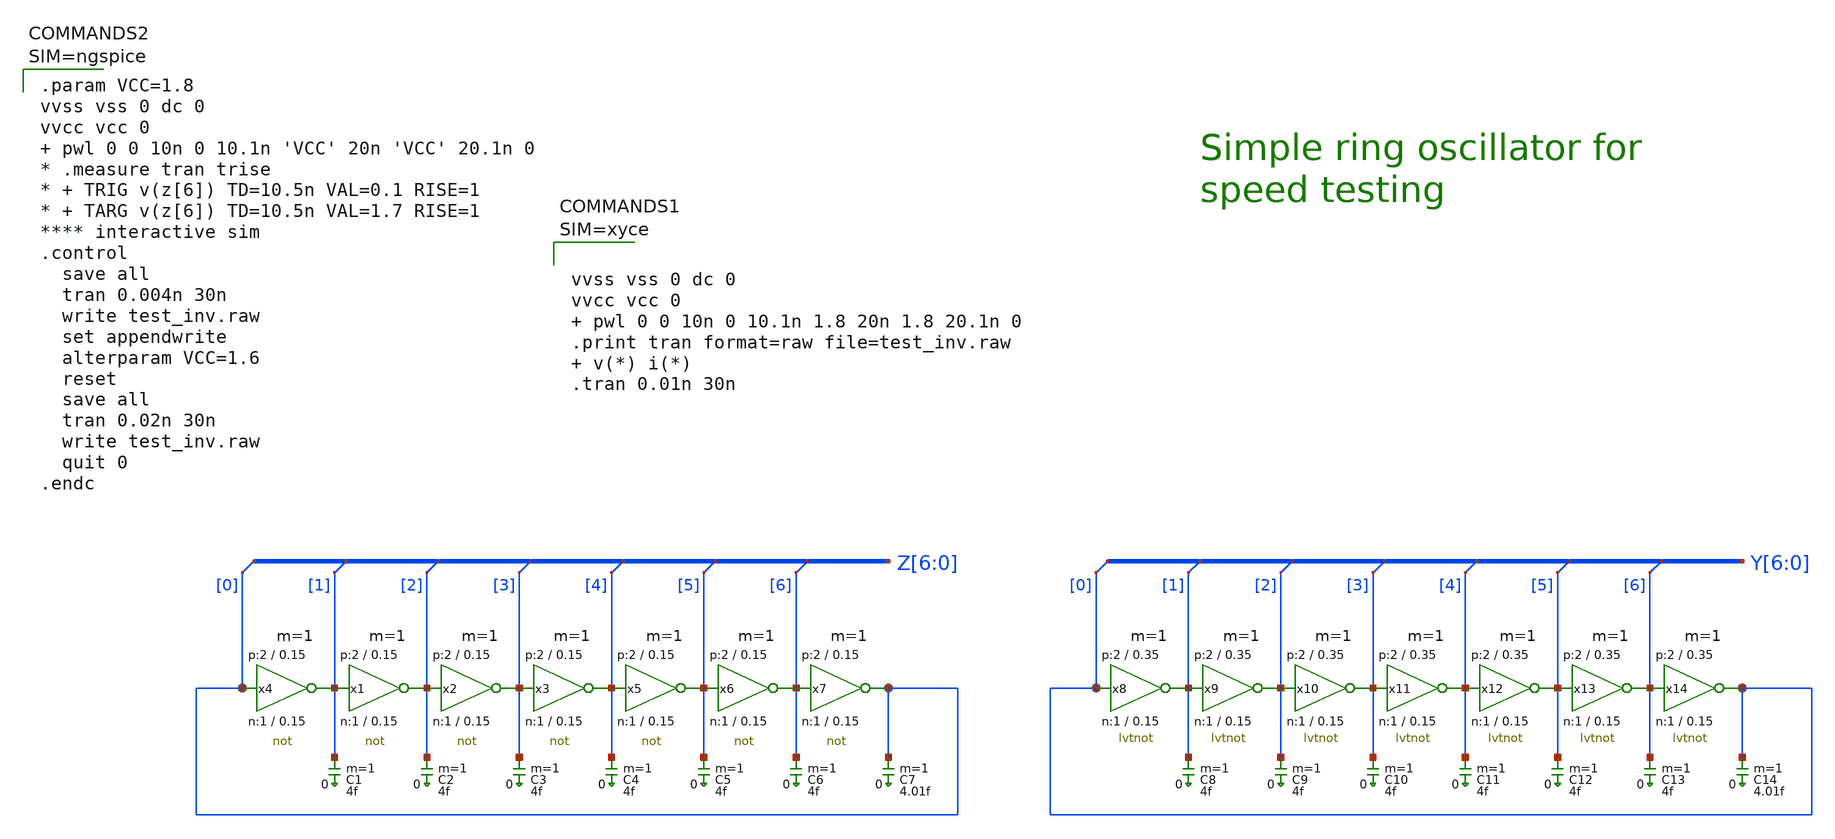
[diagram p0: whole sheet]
** sch_path: sky130_tests/test_inv.sch
* Copyright 2021 Stefan Frederik Schippers
* Licensed under the Apache License, Version 2.0 (the "License");
* you may not use this file except in compliance with the License.
* You may obtain a copy of the License at
* https://www.apache.org/licenses/LICENSE-2.0
* Unless required by applicable law or agreed to in writing, software
* distributed under the License is distributed on an "AS IS" BASIS,
* WITHOUT WARRANTIES OR CONDITIONS OF ANY KIND, either express or implied.
* See the License for the specific language governing permissions and
* limitations under the License.
**.subckt test_inv
C1 Z[1] 0 4f m=1
C2 Z[2] 0 4f m=1
C3 Z[3] 0 4f m=1
C4 Z[4] 0 4f m=1
C5 Z[5] 0 4f m=1
C6 Z[6] 0 4f m=1
C7 Z[0] 0 4.01f m=1
C8 Y[1] 0 4f m=1
C9 Y[2] 0 4f m=1
C10 Y[3] 0 4f m=1
C11 Y[4] 0 4f m=1
C12 Y[5] 0 4f m=1
C13 Y[6] 0 4f m=1
C14 Y[0] 0 4.01f m=1
x4 Z[1] Z[0] VCC VSS not W_N=1 L_N=0.15 W_P=2 L_P=0.15 m=1
x1 Z[2] Z[1] VCC VSS not W_N=1 L_N=0.15 W_P=2 L_P=0.15 m=1
x2 Z[3] Z[2] VCC VSS not W_N=1 L_N=0.15 W_P=2 L_P=0.15 m=1
x3 Z[4] Z[3] VCC VSS not W_N=1 L_N=0.15 W_P=2 L_P=0.15 m=1
x5 Z[5] Z[4] VCC VSS not W_N=1 L_N=0.15 W_P=2 L_P=0.15 m=1
x6 Z[6] Z[5] VCC VSS not W_N=1 L_N=0.15 W_P=2 L_P=0.15 m=1
x7 Z[0] Z[6] VCC VSS not W_N=1 L_N=0.15 W_P=2 L_P=0.15 m=1
x8 Y[1] Y[0] VCC VSS lvtnot W_N=1 L_N=0.15 W_P=2 L_P=0.35 m=1
x9 Y[2] Y[1] VCC VSS lvtnot W_N=1 L_N=0.15 W_P=2 L_P=0.35 m=1
x10 Y[3] Y[2] VCC VSS lvtnot W_N=1 L_N=0.15 W_P=2 L_P=0.35 m=1
x11 Y[4] Y[3] VCC VSS lvtnot W_N=1 L_N=0.15 W_P=2 L_P=0.35 m=1
x12 Y[5] Y[4] VCC VSS lvtnot W_N=1 L_N=0.15 W_P=2 L_P=0.35 m=1
x13 Y[6] Y[5] VCC VSS lvtnot W_N=1 L_N=0.15 W_P=2 L_P=0.35 m=1
x14 Y[0] Y[6] VCC VSS lvtnot W_N=1 L_N=0.15 W_P=2 L_P=0.35 m=1
* tap: Z[6:0] --> Z[0]
* tap: Z[6:0] --> Z[1]
* tap: Z[6:0] --> Z[2]
* tap: Z[6:0] --> Z[3]
* tap: Z[6:0] --> Z[4]
* tap: Z[6:0] --> Z[5]
* tap: Z[6:0] --> Z[6]
* tap: Y[6:0] --> Y[0]
* tap: Y[6:0] --> Y[1]
* tap: Y[6:0] --> Y[2]
* tap: Y[6:0] --> Y[3]
* tap: Y[6:0] --> Y[4]
* tap: Y[6:0] --> Y[5]
* tap: Y[6:0] --> Y[6]
**** begin user architecture code


.param VCC=1.8
vvss vss 0 dc 0
vvcc vcc 0   pwl 0 0 10n 0 10.1n 'VCC' 20n 'VCC' 20.1n 0
* .measure tran trise
* + TRIG v(z[6]) TD=10.5n VAL=0.1 RISE=1
* + TARG v(z[6]) TD=10.5n VAL=1.7 RISE=1
**** interactive sim
.control
  save all
  tran 0.004n 30n
  write test_inv.raw
  set appendwrite
  alterparam VCC=1.6
  reset
  save all
  tran 0.02n 30n
  write test_inv.raw
  quit 0
.endc







** opencircuitdesign pdks install
.lib $::SKYWATER_MODELS/sky130.lib.spice tt


**** end user architecture code
**.ends
.end
